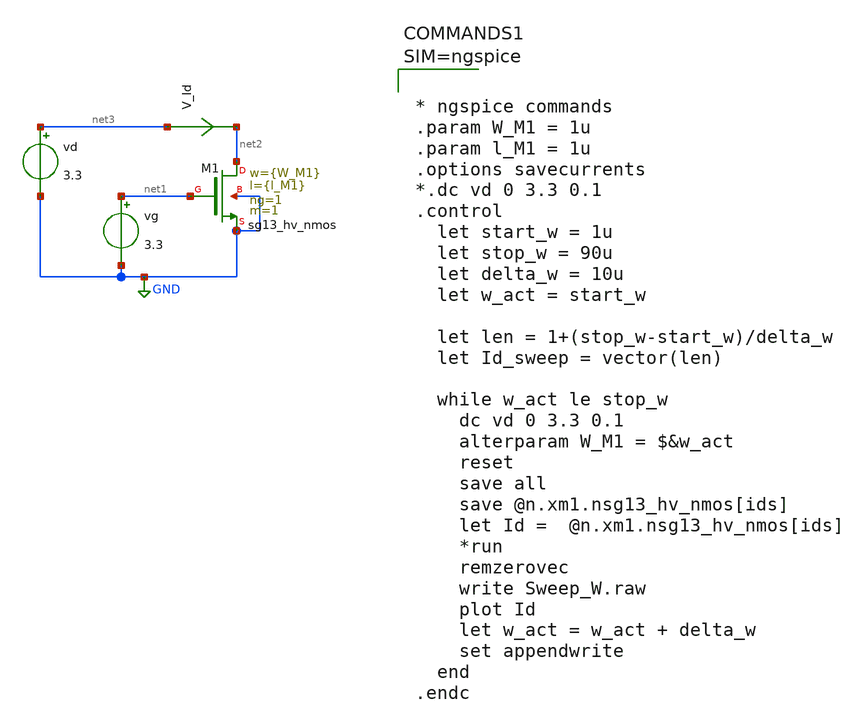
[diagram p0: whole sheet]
** sch_path: xschem/Tutorial_xschem_ngspice/Sweep_W.sch
**.subckt Sweep_W
vd net3 GND 3.3
vg net1 GND 3.3
XM1 net2 net1 GND GND sg13_hv_nmos w={W_M1} l={l_M1} ng=1 m=1 mm_ok=1
V_Id net3 net2 0
.save i(v_id)
**** begin user architecture code


.lib cornerMOShv.lib mos_tt
.lib cornerMOSlv.lib mos_tt
*.lib cornerMOShv.lib mos_ff
*.lib cornerMOSlv.lib mos_ff
*.lib cornerMOShv.lib mos_ss
*.lib cornerMOSlv.lib mos_ss
*.lib cornerMOShv.lib mos_sf
*.lib cornerMOSlv.lib mos_sf
*.lib cornerMOShv.lib mos_fs
*.lib cornerMOSlv.lib mos_fs

*.include /opt/pdks/ihp-sg13g2/libs.ref/sg13g2_stdcell/spice/sg13g2_stdcell.spice
*.lib $::SG13G2_MODELS/cornerRES.lib res_typ
*.lib $::SG13G2_MODELS/cornerCAP.lib cap_typ
*.lib $::SG13G2_MODELS/diodes.lib




* ngspice commands
.param W_M1 = 1u
.param l_M1 = 1u
.options savecurrents
*.dc vd 0 3.3 0.1
.control
  let start_w = 1u
  let stop_w = 90u
  let delta_w = 10u
  let w_act = start_w

  let len = 1+(stop_w-start_w)/delta_w
  let Id_sweep = vector(len)

  while w_act le stop_w
    dc vd 0 3.3 0.1
    alterparam W_M1 = $&w_act
    reset
    save all
    save @n.xm1.nsg13_hv_nmos[ids]
    let Id =  @n.xm1.nsg13_hv_nmos[ids]
    *run
    remzerovec
    write Sweep_W.raw
    plot Id
    let w_act = w_act + delta_w
    set appendwrite
  end
.endc



**** end user architecture code
**.ends
.GLOBAL GND
.end
